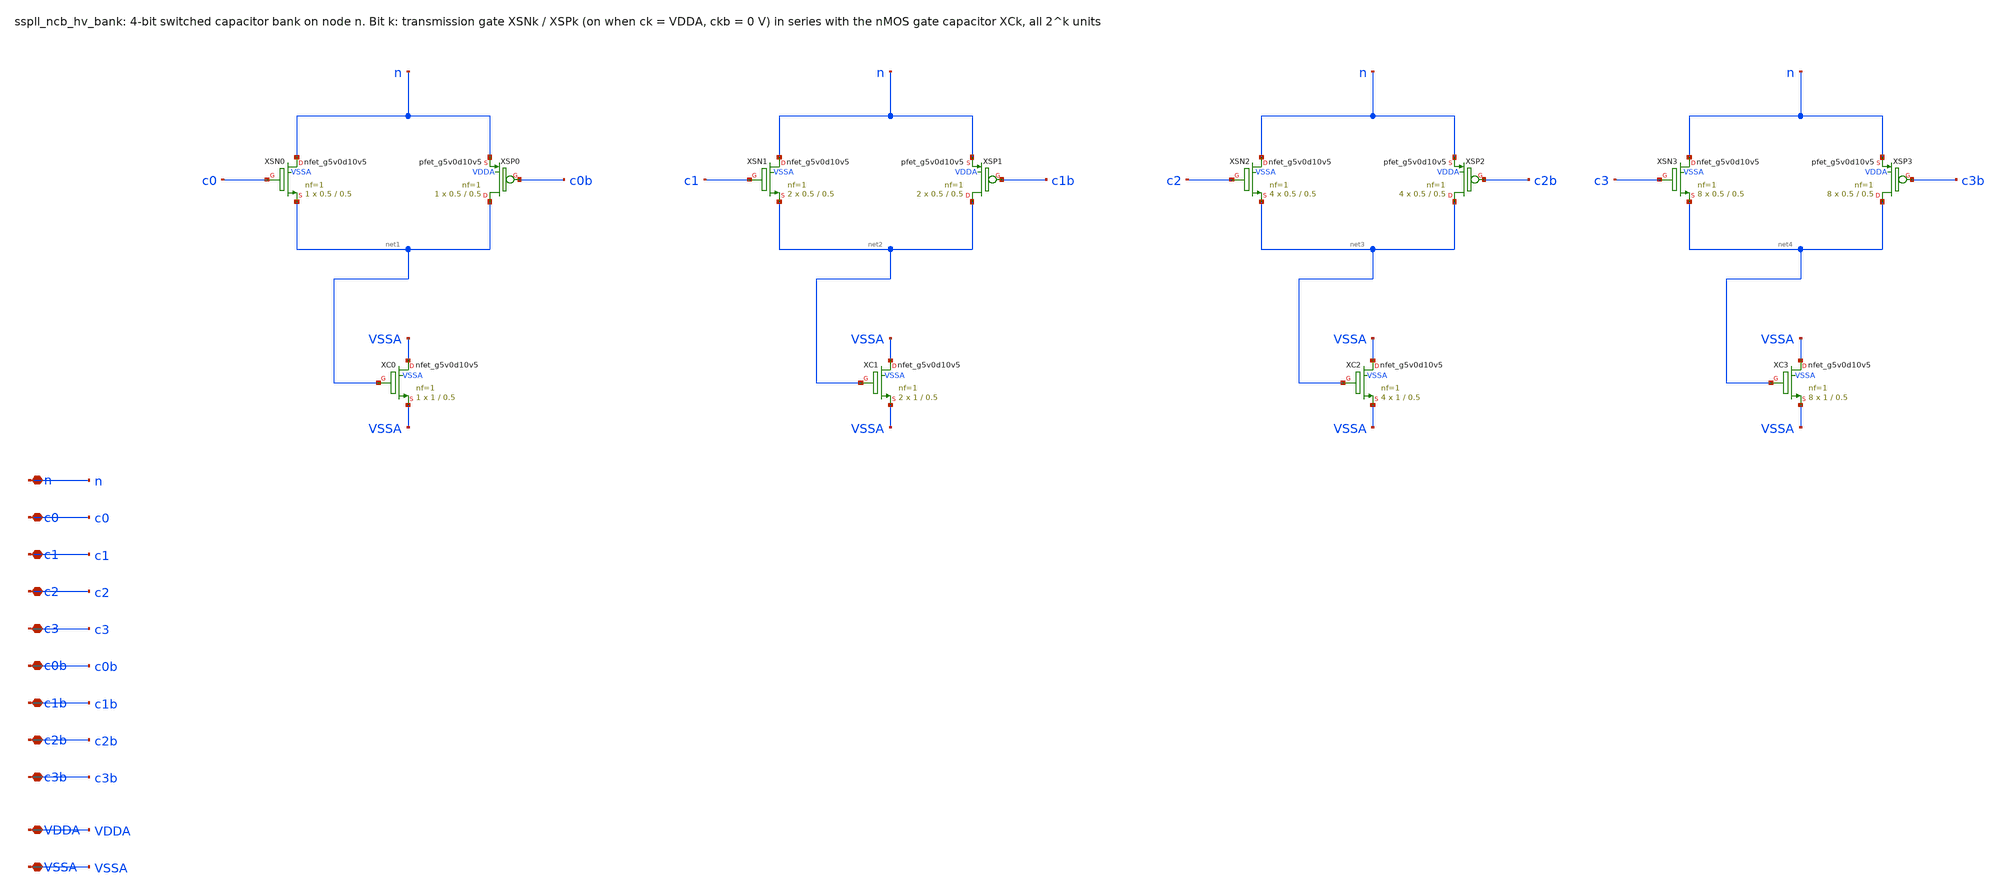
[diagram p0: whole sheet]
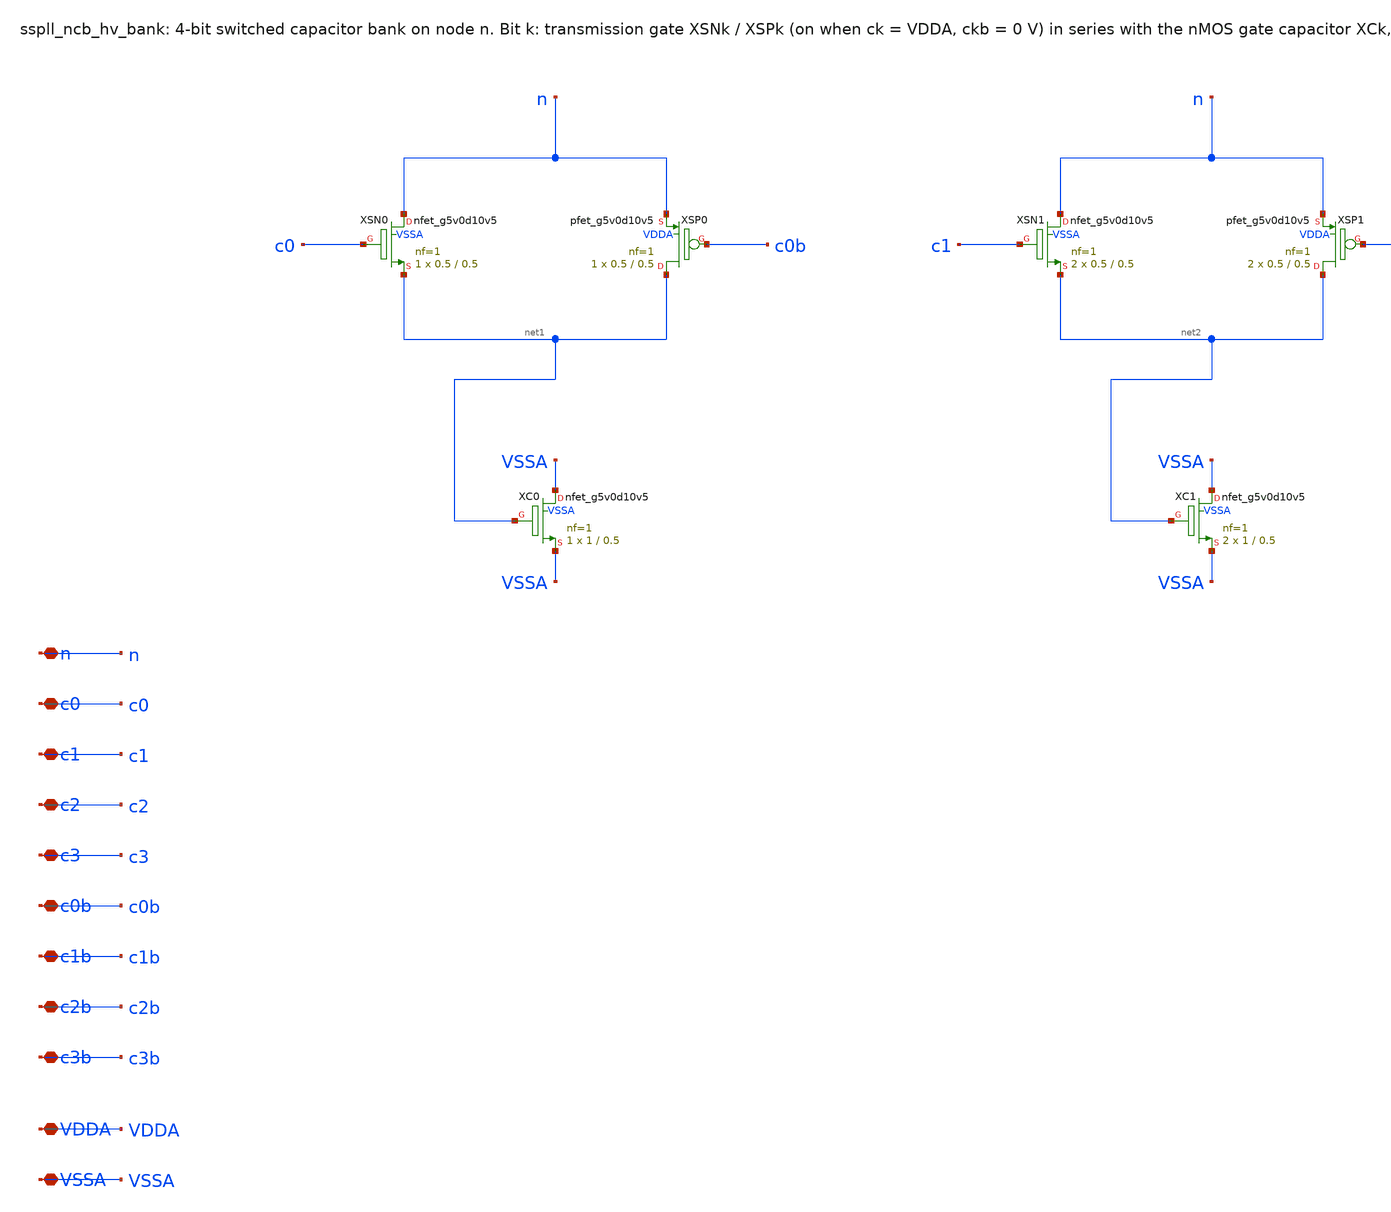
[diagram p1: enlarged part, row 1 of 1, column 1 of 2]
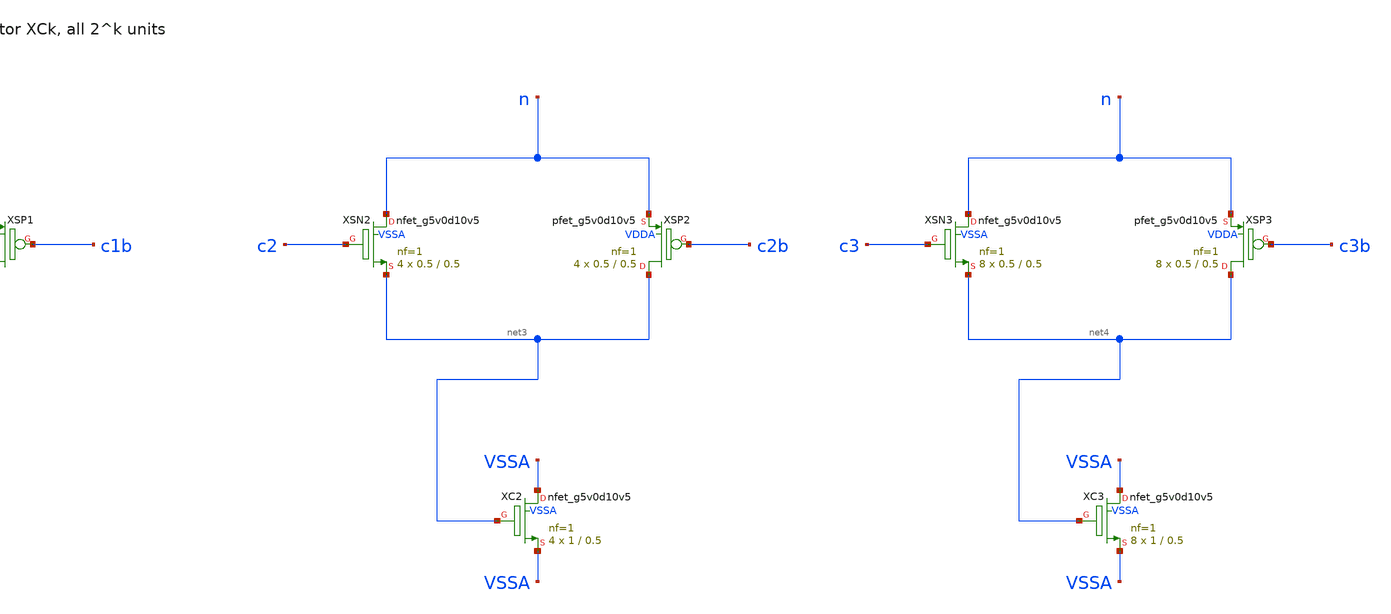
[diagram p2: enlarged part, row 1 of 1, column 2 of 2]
** sch_path: xschem/ncb_hv/sspll_ncb_hv_bank.sch
**.subckt sspll_ncb_hv_bank n c0 c1 c2 c3 c0b c1b c2b c3b VDDA VSSA
*.iopin n
*.iopin c0
*.iopin c1
*.iopin c2
*.iopin c3
*.iopin c0b
*.iopin c1b
*.iopin c2b
*.iopin c3b
*.iopin VDDA
*.iopin VSSA
XXSN0 n c0 net1 VSSA sky130_fd_pr__nfet_g5v0d10v5 L=0.5 W=0.5 nf=1 ad='int((nf+1)/2) * W/nf * 0.29' as='int((nf+2)/2) * W/nf * 0.29'
+ pd='2*int((nf+1)/2) * (W/nf + 0.29)' ps='2*int((nf+2)/2) * (W/nf + 0.29)' nrd='0.29 / W' nrs='0.29 / W'
+ sa=0 sb=0 sd=0 mult=1 m=1
XXSP0 net1 c0b n VDDA sky130_fd_pr__pfet_g5v0d10v5 L=0.5 W=0.5 nf=1 ad='int((nf+1)/2) * W/nf * 0.29'
+ as='int((nf+2)/2) * W/nf * 0.29' pd='2*int((nf+1)/2) * (W/nf + 0.29)' ps='2*int((nf+2)/2) * (W/nf + 0.29)'
+ nrd='0.29 / W' nrs='0.29 / W' sa=0 sb=0 sd=0 mult=1 m=1
XXC0 VSSA net1 VSSA VSSA sky130_fd_pr__nfet_g5v0d10v5 L=0.5 W=1 nf=1 ad='int((nf+1)/2) * W/nf * 0.29'
+ as='int((nf+2)/2) * W/nf * 0.29' pd='2*int((nf+1)/2) * (W/nf + 0.29)' ps='2*int((nf+2)/2) * (W/nf + 0.29)'
+ nrd='0.29 / W' nrs='0.29 / W' sa=0 sb=0 sd=0 mult=1 m=1
XXSN1 n c1 net2 VSSA sky130_fd_pr__nfet_g5v0d10v5 L=0.5 W=0.5 nf=1 ad='int((nf+1)/2) * W/nf * 0.29' as='int((nf+2)/2) * W/nf * 0.29'
+ pd='2*int((nf+1)/2) * (W/nf + 0.29)' ps='2*int((nf+2)/2) * (W/nf + 0.29)' nrd='0.29 / W' nrs='0.29 / W'
+ sa=0 sb=0 sd=0 mult=2 m=2
XXSP1 net2 c1b n VDDA sky130_fd_pr__pfet_g5v0d10v5 L=0.5 W=0.5 nf=1 ad='int((nf+1)/2) * W/nf * 0.29'
+ as='int((nf+2)/2) * W/nf * 0.29' pd='2*int((nf+1)/2) * (W/nf + 0.29)' ps='2*int((nf+2)/2) * (W/nf + 0.29)'
+ nrd='0.29 / W' nrs='0.29 / W' sa=0 sb=0 sd=0 mult=2 m=2
XXC1 VSSA net2 VSSA VSSA sky130_fd_pr__nfet_g5v0d10v5 L=0.5 W=1 nf=1 ad='int((nf+1)/2) * W/nf * 0.29'
+ as='int((nf+2)/2) * W/nf * 0.29' pd='2*int((nf+1)/2) * (W/nf + 0.29)' ps='2*int((nf+2)/2) * (W/nf + 0.29)'
+ nrd='0.29 / W' nrs='0.29 / W' sa=0 sb=0 sd=0 mult=2 m=2
XXSN2 n c2 net3 VSSA sky130_fd_pr__nfet_g5v0d10v5 L=0.5 W=0.5 nf=1 ad='int((nf+1)/2) * W/nf * 0.29' as='int((nf+2)/2) * W/nf * 0.29'
+ pd='2*int((nf+1)/2) * (W/nf + 0.29)' ps='2*int((nf+2)/2) * (W/nf + 0.29)' nrd='0.29 / W' nrs='0.29 / W'
+ sa=0 sb=0 sd=0 mult=4 m=4
XXSP2 net3 c2b n VDDA sky130_fd_pr__pfet_g5v0d10v5 L=0.5 W=0.5 nf=1 ad='int((nf+1)/2) * W/nf * 0.29'
+ as='int((nf+2)/2) * W/nf * 0.29' pd='2*int((nf+1)/2) * (W/nf + 0.29)' ps='2*int((nf+2)/2) * (W/nf + 0.29)'
+ nrd='0.29 / W' nrs='0.29 / W' sa=0 sb=0 sd=0 mult=4 m=4
XXC2 VSSA net3 VSSA VSSA sky130_fd_pr__nfet_g5v0d10v5 L=0.5 W=1 nf=1 ad='int((nf+1)/2) * W/nf * 0.29'
+ as='int((nf+2)/2) * W/nf * 0.29' pd='2*int((nf+1)/2) * (W/nf + 0.29)' ps='2*int((nf+2)/2) * (W/nf + 0.29)'
+ nrd='0.29 / W' nrs='0.29 / W' sa=0 sb=0 sd=0 mult=4 m=4
XXSN3 n c3 net4 VSSA sky130_fd_pr__nfet_g5v0d10v5 L=0.5 W=0.5 nf=1 ad='int((nf+1)/2) * W/nf * 0.29' as='int((nf+2)/2) * W/nf * 0.29'
+ pd='2*int((nf+1)/2) * (W/nf + 0.29)' ps='2*int((nf+2)/2) * (W/nf + 0.29)' nrd='0.29 / W' nrs='0.29 / W'
+ sa=0 sb=0 sd=0 mult=8 m=8
XXSP3 net4 c3b n VDDA sky130_fd_pr__pfet_g5v0d10v5 L=0.5 W=0.5 nf=1 ad='int((nf+1)/2) * W/nf * 0.29'
+ as='int((nf+2)/2) * W/nf * 0.29' pd='2*int((nf+1)/2) * (W/nf + 0.29)' ps='2*int((nf+2)/2) * (W/nf + 0.29)'
+ nrd='0.29 / W' nrs='0.29 / W' sa=0 sb=0 sd=0 mult=8 m=8
XXC3 VSSA net4 VSSA VSSA sky130_fd_pr__nfet_g5v0d10v5 L=0.5 W=1 nf=1 ad='int((nf+1)/2) * W/nf * 0.29'
+ as='int((nf+2)/2) * W/nf * 0.29' pd='2*int((nf+1)/2) * (W/nf + 0.29)' ps='2*int((nf+2)/2) * (W/nf + 0.29)'
+ nrd='0.29 / W' nrs='0.29 / W' sa=0 sb=0 sd=0 mult=8 m=8
**.ends
.end
